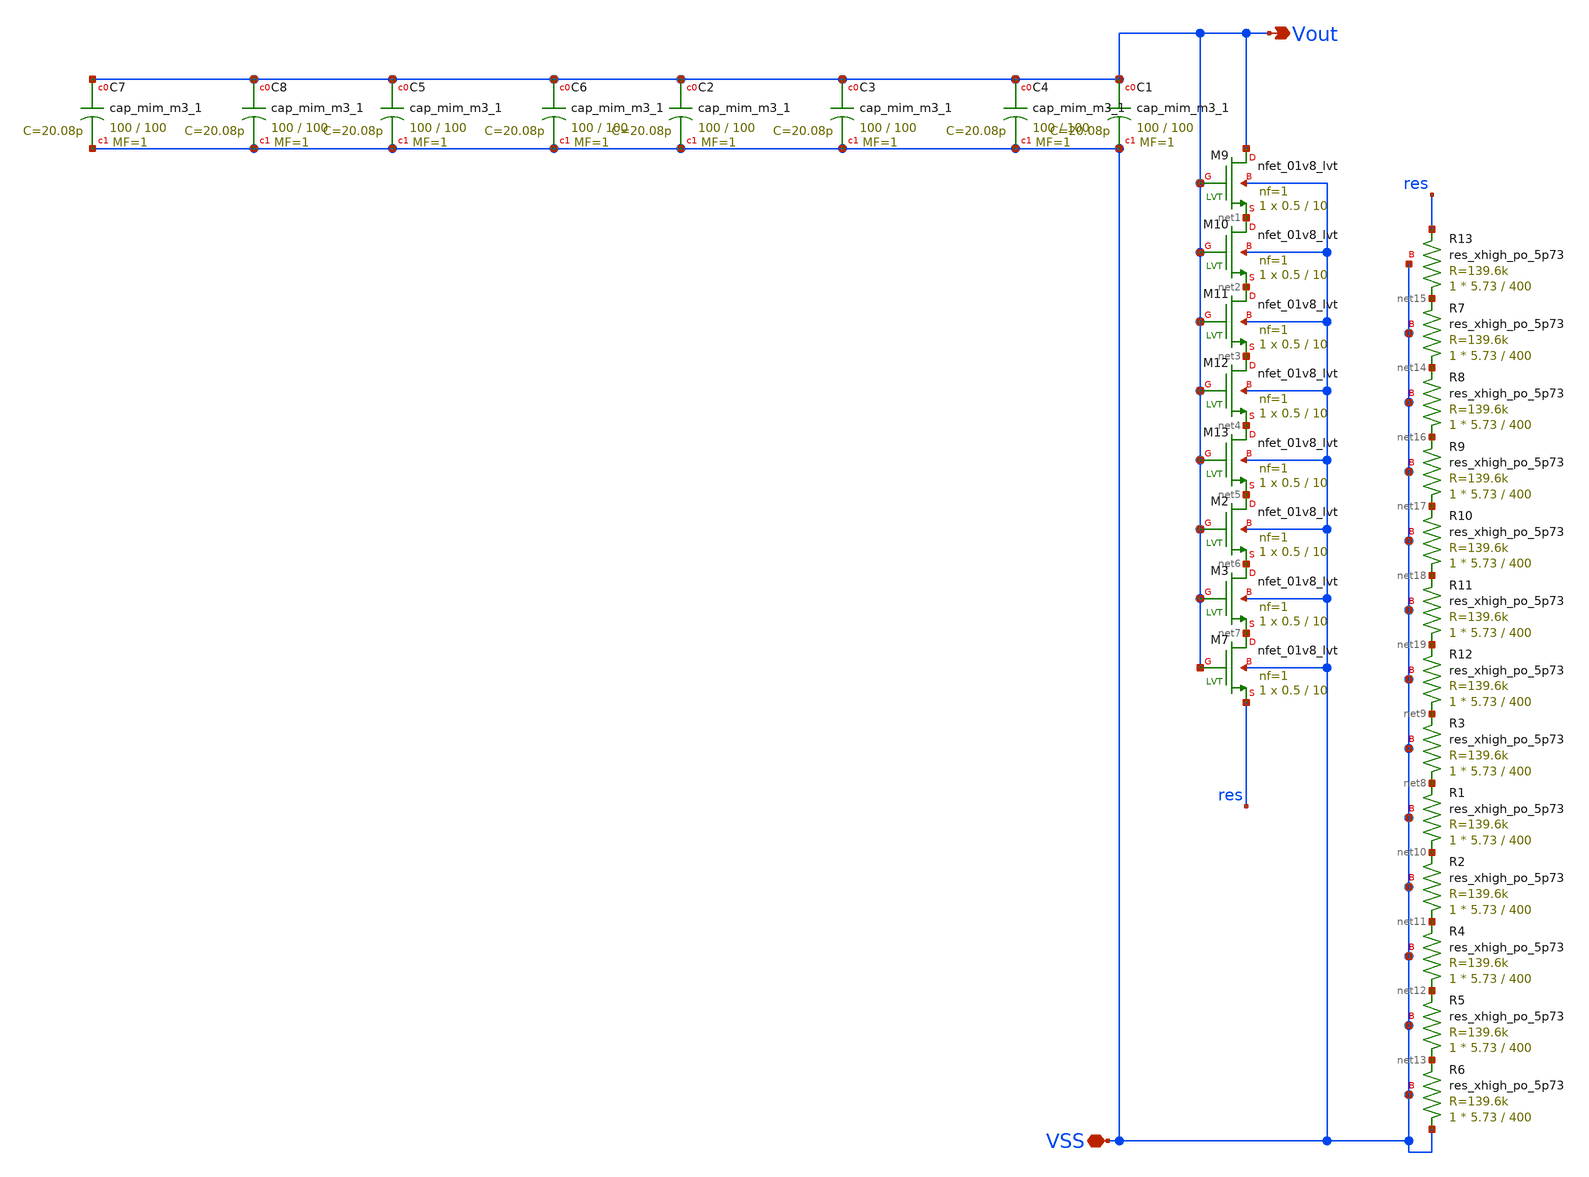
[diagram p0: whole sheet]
** sch_path: xschem/cmos_imager/photodiode_real_rc_8cap_lvs.sch
**.subckt photodiode_real_rc_8cap_lvs Vout VSS
*.opin Vout
*.iopin VSS
XC1 Vout VSS sky130_fd_pr__cap_mim_m3_1 W=100 L=100 MF=1 m=1
XM9 Vout Vout net1 VSS sky130_fd_pr__nfet_01v8_lvt L=10 W=0.5 nf=1 ad='int((nf+1)/2) * W/nf * 0.29' as='int((nf+2)/2) * W/nf * 0.29'
+ pd='2*int((nf+1)/2) * (W/nf + 0.29)' ps='2*int((nf+2)/2) * (W/nf + 0.29)' nrd='0.29 / W' nrs='0.29 / W'
+ sa=0 sb=0 sd=0 mult=1 m=1
XM10 net1 Vout net2 VSS sky130_fd_pr__nfet_01v8_lvt L=10 W=0.5 nf=1 ad='int((nf+1)/2) * W/nf * 0.29'
+ as='int((nf+2)/2) * W/nf * 0.29' pd='2*int((nf+1)/2) * (W/nf + 0.29)' ps='2*int((nf+2)/2) * (W/nf + 0.29)'
+ nrd='0.29 / W' nrs='0.29 / W' sa=0 sb=0 sd=0 mult=1 m=1
XM11 net2 Vout net3 VSS sky130_fd_pr__nfet_01v8_lvt L=10 W=0.5 nf=1 ad='int((nf+1)/2) * W/nf * 0.29'
+ as='int((nf+2)/2) * W/nf * 0.29' pd='2*int((nf+1)/2) * (W/nf + 0.29)' ps='2*int((nf+2)/2) * (W/nf + 0.29)'
+ nrd='0.29 / W' nrs='0.29 / W' sa=0 sb=0 sd=0 mult=1 m=1
XM12 net3 Vout net4 VSS sky130_fd_pr__nfet_01v8_lvt L=10 W=0.5 nf=1 ad='int((nf+1)/2) * W/nf * 0.29'
+ as='int((nf+2)/2) * W/nf * 0.29' pd='2*int((nf+1)/2) * (W/nf + 0.29)' ps='2*int((nf+2)/2) * (W/nf + 0.29)'
+ nrd='0.29 / W' nrs='0.29 / W' sa=0 sb=0 sd=0 mult=1 m=1
XM13 net4 Vout net5 VSS sky130_fd_pr__nfet_01v8_lvt L=10 W=0.5 nf=1 ad='int((nf+1)/2) * W/nf * 0.29'
+ as='int((nf+2)/2) * W/nf * 0.29' pd='2*int((nf+1)/2) * (W/nf + 0.29)' ps='2*int((nf+2)/2) * (W/nf + 0.29)'
+ nrd='0.29 / W' nrs='0.29 / W' sa=0 sb=0 sd=0 mult=1 m=1
XM2 net5 Vout net6 VSS sky130_fd_pr__nfet_01v8_lvt L=10 W=0.5 nf=1 ad='int((nf+1)/2) * W/nf * 0.29' as='int((nf+2)/2) * W/nf * 0.29'
+ pd='2*int((nf+1)/2) * (W/nf + 0.29)' ps='2*int((nf+2)/2) * (W/nf + 0.29)' nrd='0.29 / W' nrs='0.29 / W'
+ sa=0 sb=0 sd=0 mult=1 m=1
XM3 net6 Vout net7 VSS sky130_fd_pr__nfet_01v8_lvt L=10 W=0.5 nf=1 ad='int((nf+1)/2) * W/nf * 0.29' as='int((nf+2)/2) * W/nf * 0.29'
+ pd='2*int((nf+1)/2) * (W/nf + 0.29)' ps='2*int((nf+2)/2) * (W/nf + 0.29)' nrd='0.29 / W' nrs='0.29 / W'
+ sa=0 sb=0 sd=0 mult=1 m=1
XM7 net7 Vout res VSS sky130_fd_pr__nfet_01v8_lvt L=10 W=0.5 nf=1 ad='int((nf+1)/2) * W/nf * 0.29' as='int((nf+2)/2) * W/nf * 0.29'
+ pd='2*int((nf+1)/2) * (W/nf + 0.29)' ps='2*int((nf+2)/2) * (W/nf + 0.29)' nrd='0.29 / W' nrs='0.29 / W'
+ sa=0 sb=0 sd=0 mult=1 m=1
XR3 net8 net9 VSS sky130_fd_pr__res_xhigh_po_5p73 L=400 mult=1 m=1
XR1 net10 net8 VSS sky130_fd_pr__res_xhigh_po_5p73 L=400 mult=1 m=1
XR2 net11 net10 VSS sky130_fd_pr__res_xhigh_po_5p73 L=400 mult=1 m=1
XR4 net12 net11 VSS sky130_fd_pr__res_xhigh_po_5p73 L=400 mult=1 m=1
XR5 net13 net12 VSS sky130_fd_pr__res_xhigh_po_5p73 L=400 mult=1 m=1
XR6 VSS net13 VSS sky130_fd_pr__res_xhigh_po_5p73 L=400 mult=1 m=1
XR7 net14 net15 VSS sky130_fd_pr__res_xhigh_po_5p73 L=400 mult=1 m=1
XR8 net16 net14 VSS sky130_fd_pr__res_xhigh_po_5p73 L=400 mult=1 m=1
XR9 net17 net16 VSS sky130_fd_pr__res_xhigh_po_5p73 L=400 mult=1 m=1
XR10 net18 net17 VSS sky130_fd_pr__res_xhigh_po_5p73 L=400 mult=1 m=1
XR11 net19 net18 VSS sky130_fd_pr__res_xhigh_po_5p73 L=400 mult=1 m=1
XR12 net9 net19 VSS sky130_fd_pr__res_xhigh_po_5p73 L=400 mult=1 m=1
XR13 net15 res VSS sky130_fd_pr__res_xhigh_po_5p73 L=400 mult=1 m=1
XC2 Vout VSS sky130_fd_pr__cap_mim_m3_1 W=100 L=100 MF=1 m=1
XC3 Vout VSS sky130_fd_pr__cap_mim_m3_1 W=100 L=100 MF=1 m=1
XC4 Vout VSS sky130_fd_pr__cap_mim_m3_1 W=100 L=100 MF=1 m=1
XC5 Vout VSS sky130_fd_pr__cap_mim_m3_1 W=100 L=100 MF=1 m=1
XC6 Vout VSS sky130_fd_pr__cap_mim_m3_1 W=100 L=100 MF=1 m=1
XC7 Vout VSS sky130_fd_pr__cap_mim_m3_1 W=100 L=100 MF=1 m=1
XC8 Vout VSS sky130_fd_pr__cap_mim_m3_1 W=100 L=100 MF=1 m=1
**.ends
.end
